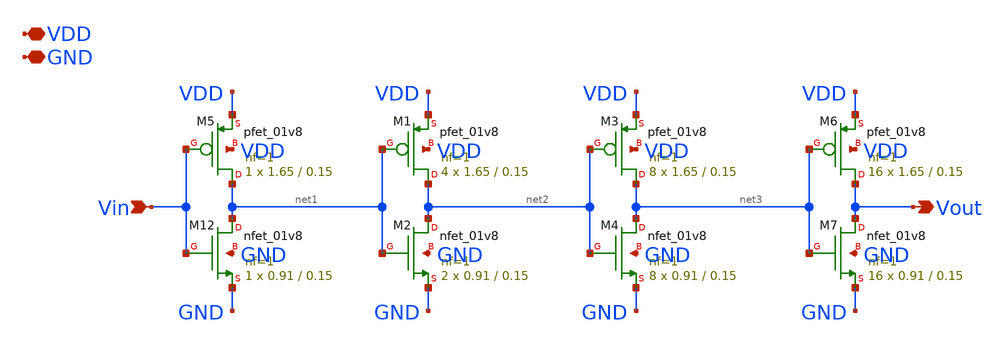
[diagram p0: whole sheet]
** sch_path: xschem/capswitch16.sch
**.subckt capswitch16 Vin Vout VDD GND
*.ipin Vin
*.opin Vout
*.iopin VDD
*.iopin GND
XM5 net1 Vin VDD VDD sky130_fd_pr__pfet_01v8 L=0.15 W=1.65 nf=1 ad='int((nf+1)/2) * W/nf * 0.29' as='int((nf+2)/2) * W/nf * 0.29'
+ pd='2*int((nf+1)/2) * (W/nf + 0.29)' ps='2*int((nf+2)/2) * (W/nf + 0.29)' nrd='0.29 / W' nrs='0.29 / W'
+ sa=0 sb=0 sd=0 mult=1 m=1
XM12 net1 Vin GND GND sky130_fd_pr__nfet_01v8 L=0.15 W=0.91 nf=1 ad='int((nf+1)/2) * W/nf * 0.29' as='int((nf+2)/2) * W/nf * 0.29'
+ pd='2*int((nf+1)/2) * (W/nf + 0.29)' ps='2*int((nf+2)/2) * (W/nf + 0.29)' nrd='0.29 / W' nrs='0.29 / W'
+ sa=0 sb=0 sd=0 mult=1 m=1
XM1 net2 net1 VDD VDD sky130_fd_pr__pfet_01v8 L=0.15 W=1.65 nf=1 ad='int((nf+1)/2) * W/nf * 0.29' as='int((nf+2)/2) * W/nf * 0.29'
+ pd='2*int((nf+1)/2) * (W/nf + 0.29)' ps='2*int((nf+2)/2) * (W/nf + 0.29)' nrd='0.29 / W' nrs='0.29 / W'
+ sa=0 sb=0 sd=0 mult=4 m=4
XM2 net2 net1 GND GND sky130_fd_pr__nfet_01v8 L=0.15 W=0.91 nf=1 ad='int((nf+1)/2) * W/nf * 0.29' as='int((nf+2)/2) * W/nf * 0.29'
+ pd='2*int((nf+1)/2) * (W/nf + 0.29)' ps='2*int((nf+2)/2) * (W/nf + 0.29)' nrd='0.29 / W' nrs='0.29 / W'
+ sa=0 sb=0 sd=0 mult=2 m=2
XM3 net3 net2 VDD VDD sky130_fd_pr__pfet_01v8 L=0.15 W=1.65 nf=1 ad='int((nf+1)/2) * W/nf * 0.29' as='int((nf+2)/2) * W/nf * 0.29'
+ pd='2*int((nf+1)/2) * (W/nf + 0.29)' ps='2*int((nf+2)/2) * (W/nf + 0.29)' nrd='0.29 / W' nrs='0.29 / W'
+ sa=0 sb=0 sd=0 mult=8 m=8
XM4 net3 net2 GND GND sky130_fd_pr__nfet_01v8 L=0.15 W=0.91 nf=1 ad='int((nf+1)/2) * W/nf * 0.29' as='int((nf+2)/2) * W/nf * 0.29'
+ pd='2*int((nf+1)/2) * (W/nf + 0.29)' ps='2*int((nf+2)/2) * (W/nf + 0.29)' nrd='0.29 / W' nrs='0.29 / W'
+ sa=0 sb=0 sd=0 mult=8 m=8
XM6 Vout net3 VDD VDD sky130_fd_pr__pfet_01v8 L=0.15 W=1.65 nf=1 ad='int((nf+1)/2) * W/nf * 0.29' as='int((nf+2)/2) * W/nf * 0.29'
+ pd='2*int((nf+1)/2) * (W/nf + 0.29)' ps='2*int((nf+2)/2) * (W/nf + 0.29)' nrd='0.29 / W' nrs='0.29 / W'
+ sa=0 sb=0 sd=0 mult=16 m=16
XM7 Vout net3 GND GND sky130_fd_pr__nfet_01v8 L=0.15 W=0.91 nf=1 ad='int((nf+1)/2) * W/nf * 0.29' as='int((nf+2)/2) * W/nf * 0.29'
+ pd='2*int((nf+1)/2) * (W/nf + 0.29)' ps='2*int((nf+2)/2) * (W/nf + 0.29)' nrd='0.29 / W' nrs='0.29 / W'
+ sa=0 sb=0 sd=0 mult=16 m=16
**.ends
.end
